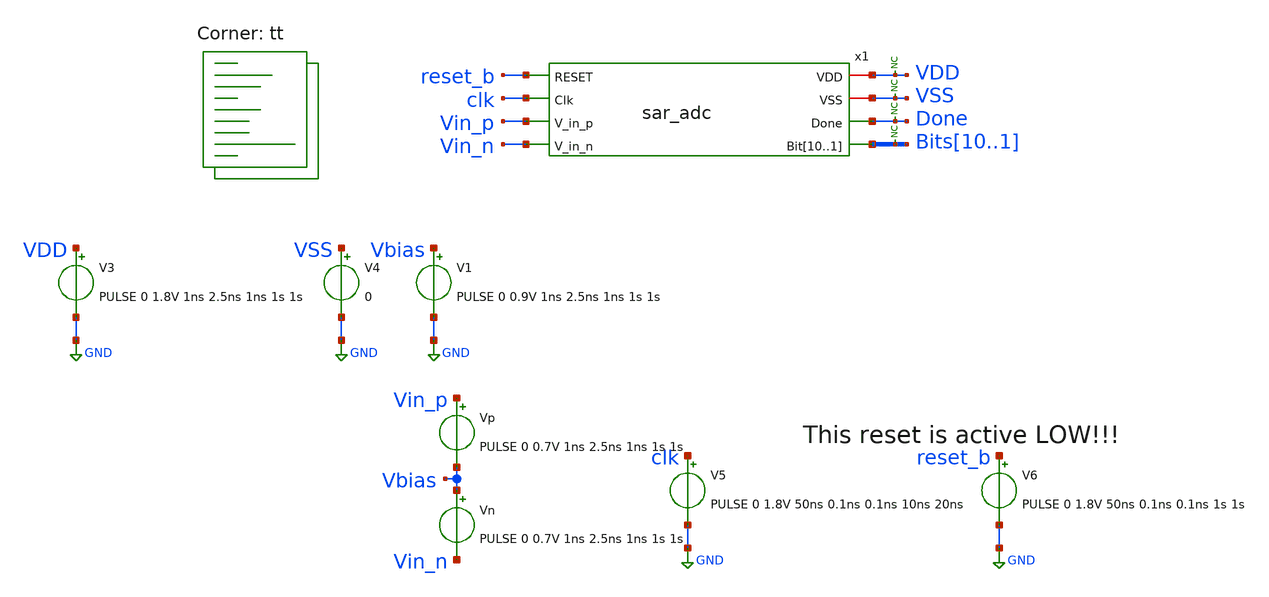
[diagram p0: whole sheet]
** sch_path: xschem/tests/sar_adc/sar_adc_sine_max_sample_test.sch
**.subckt sar_adc_sine_max_sample_test
V3 VDD GND PULSE 0 1.8V 1ns 2.5ns 1ns 1s 1s
V4 VSS GND 0
x1 VDD VSS reset_b clk Vin_p Vin_n Done Bits10 Bits9 Bits8 Bits7 Bits6 Bits5 Bits4 Bits3 Bits2 Bits1
+ sar_adc
V1 Vbias GND PULSE 0 0.9V 1ns 2.5ns 1ns 1s 1s
* noconn VDD
* noconn VSS
* noconn Done
* noconn Bits[10..1]
Vn Vbias Vin_n PULSE 0 0.7V 1ns 2.5ns 1ns 1s 1s
V5 clk GND PULSE 0 1.8V 50ns 0.1ns 0.1ns 10ns 20ns
V6 reset_b GND PULSE 0 1.8V 50ns 0.1ns 0.1ns 1s 1s
Vp Vin_p Vbias PULSE 0 0.7V 1ns 2.5ns 1ns 1s 1s
**** begin user architecture code

*.lib $::SKYWATER_MODELS/sky130.lib.spice tt

* .lib $::SKYWATER_MODELS/sky130.lib.spice.tt.red tt

.include $::SKYWATER_STDCELLS/sky130_fd_sc_hd.spice

.lib $::SKYWATER_MODELS/sky130.lib.spice tt



* Requires an iterator variable to be passed in!
* Simulation calculates (steps_per_iter) bits of
* a sine wave at times shifted by (iterator)

* Coherent sampling Set for
* 4 Sigfigs
* 3.125e3 sample rate
* 1e3 input freq

* ngspice commands
.options list acct opts
.options method=gear
.control
save all
* Go to the const plot
setplot const

let steps_per_iter = 4
let total_runs = $&steps_per_iter
let runs = 0
let all_runs = $iterator * $&total_runs
let runs_start = $&all_runs
let phase_offset = 0.1

* These are the coherent values
let sample_period = 640.3689e-9
let source_freq = 506.3e3

let vdiff = 0.9 * sin(2 * $&pi * $&source_freq * $&sample_period * $&all_runs + $&phase_offset)
let vstart = $&vdiff


let out_bits = vector($&total_runs*10)
reshape out_bits[10][$&total_runs]
let in_diff_v= vector($&total_runs)
let vsampled_p = vector($&total_runs)
let vsampled_n = vector($&total_runs)
let sample_times = vector($&total_runs)

echo
echo AWS iterator = $iterator
echo vdiff = $&vdiff
echo steps_per_iter = $&steps_per_iter
echo total_runs = $&total_runs
echo runs = $&runs
echo

* Insert vector names and set only one scale
set wr_vecnames
set wr_singlescale

* set the hcopy type
set hcopydevtype=svg


while $&runs lt $&total_runs
	echo
	echo run = $&runs
	echo Vdiff = $&vdiff
	echo
	* Alter the voltages
	alter \@Vp[pulse] = [ 0 $&vdiff 1n 2.5n 1n 1 1 ] $ vector
	alter \@Vn[pulse] = [ 0 $&vdiff 1n 2.5n 1n 1 1 ] $ vector

	* Run the tran
	* tran creates a new plot starting with tran1
	tran 0.5n 700n uic

	set pltfile1 = plot_converg_{$&all_runs}_{$&vdiff}.svg
	set pltfile2 = plot_input_v_{$&all_runs}_{$&vdiff}.svg
	set pltfile3 = plot_clks_{$&all_runs}_{$&vdiff}.svg
	set plttitle = run{$&all_runs}_vin{$&vdiff}
	hardcopy $pltfile1 x1.vsampled_p x1.vsampled_n x1.vsampled_p-x1.vsampled_n x1.sw_sample-2
+ x1.comp_out_p+2 x1.comp_out_n-2 title $plttitle
	*hardcopy $pltfile2 vin_p vin_n vss vdd vbias title $plttitle
	hardcopy $pltfile3 x1.x1.cycle0 x1.x1.cycle1 x1.x1.cycle2 x1.x1.cycle3 x1.x1.cycle4 x1.x1.cycle5
+ x1.x1.cycle6 x1.x1.cycle7 x1.x1.cycle8 x1.x1.cycle9 x1.x1.cycle10 x1.x1.cycle11 x1.x1.cycle12 x1.x1.cycle13
+ x1.x1.cycle14 x1.x1.cycle15 x1.controller_clk+2 title $plttitle



	* Measure the max to find the output
	meas tran max_bit0 MAX v(bits1) from=650n to=655n
	meas tran max_bit1 MAX v(bits2) from=650n to=655n
	meas tran max_bit2 MAX v(bits3) from=650n to=655n
	meas tran max_bit3 MAX v(bits4) from=650n to=655n
	meas tran max_bit4 MAX v(bits5) from=650n to=655n
	meas tran max_bit5 MAX v(bits6) from=650n to=655n
	meas tran max_bit6 MAX v(bits7) from=650n to=655n
	meas tran max_bit7 MAX v(bits8) from=650n to=655n
	meas tran max_bit8 MAX v(bits9) from=650n to=655n
	meas tran max_bit9 MAX v(bits10) from=650n to=655n
	meas tran avg_vsampled_p AVG v(x1.vsampled_p) from=605n to=610n
	meas tran avg_vsampled_n AVG v(x1.vsampled_n) from=605n to=610n


	* Create variables
	set max_bit0 = $&max_bit0
	set max_bit1 = $&max_bit1
	set max_bit2 = $&max_bit2
	set max_bit3 = $&max_bit3
	set max_bit4 = $&max_bit4
	set max_bit5 = $&max_bit5
	set max_bit6 = $&max_bit6
	set max_bit7 = $&max_bit7
	set max_bit8 = $&max_bit8
	set max_bit9 = $&max_bit9
	set vdiff = $&vdiff
	set vsampled_p = $&avg_vsampled_p
	set vsampled_n = $&avg_vsampled_n
	let this_sample_time = $&sample_period * $&all_runs
	set this_sample_time = $&this_sample_time

	* Switch to constants plot
	setplot const
	*compose out_bits values $&out_bits $p_max $n_max
	let in_diff_v[$&runs] = $vdiff
	let vsampled_p[$&runs] = $vsampled_p
	let vsampled_n[$&runs] = $vsampled_n
	let sample_times[$&runs] = $this_sample_time
	let out_bits[0][$&runs] = $max_bit0
	let out_bits[1][$&runs] = $max_bit1
	let out_bits[2][$&runs] = $max_bit2
	let out_bits[3][$&runs] = $max_bit3
	let out_bits[4][$&runs] = $max_bit4
	let out_bits[5][$&runs] = $max_bit5
	let out_bits[6][$&runs] = $max_bit6
	let out_bits[7][$&runs] = $max_bit7
	let out_bits[8][$&runs] = $max_bit8
	let out_bits[9][$&runs] = $max_bit9

	* set the iterators
	echo run $&runs
	let runs = runs + 1
	let all_runs = all_runs + 1
	let vdiff = 0.9 * sin(2 * $&pi * $&source_freq * $&sample_period * $&all_runs + $&phase_offset)

	* Destroy the transient plot to release memory
	destroy tran1

end

* switch to the const plot
setplot const
compose def_scale start=1 stop=$&total_runs step=1
setscale def_scale
echo Writing out_bits.txt
wrdata out_bits.txt vsampled_p vsampled_n in_diff_v out_bits sample_times

echo
echo Total Runs = $&runs
echo Run from = $&runs_start to = $&all_runs
echo
.endc



**** end user architecture code
**.ends
.GLOBAL GND
.end
